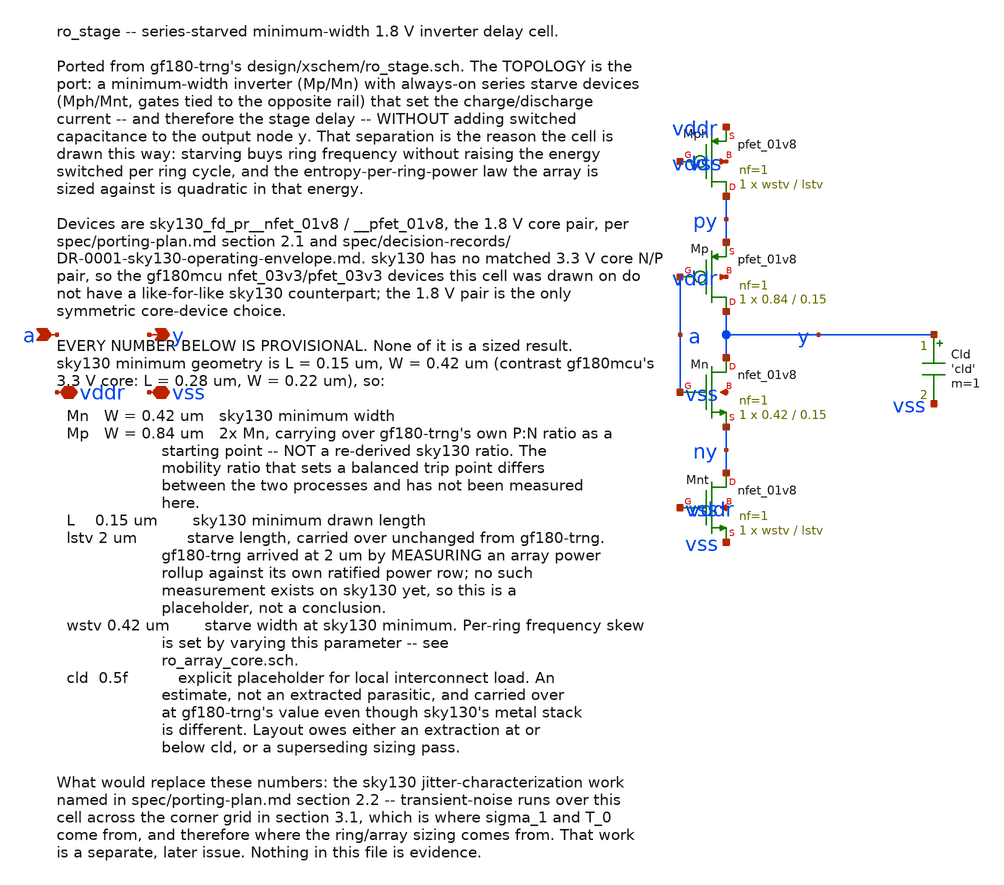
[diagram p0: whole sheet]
** sch_path: design/xschem/ro_stage.sch
**.subckt ro_stage a y vddr vss
*.ipin a
*.opin y
*.iopin vddr
*.iopin vss
XMph py vss vddr vddr sky130_fd_pr__pfet_01v8 L=lstv W=wstv nf=1 ad='int((nf+1)/2) * W/nf * 0.29' as='int((nf+2)/2) * W/nf * 0.29'
+ pd='2*int((nf+1)/2) * (W/nf + 0.29)' ps='2*int((nf+2)/2) * (W/nf + 0.29)' nrd='0.29 / W' nrs='0.29 / W'
+ sa=0 sb=0 sd=0 mult=1 m=1
XMp y a py vddr sky130_fd_pr__pfet_01v8 L=0.15 W=0.84 nf=1 ad='int((nf+1)/2) * W/nf * 0.29' as='int((nf+2)/2) * W/nf * 0.29'
+ pd='2*int((nf+1)/2) * (W/nf + 0.29)' ps='2*int((nf+2)/2) * (W/nf + 0.29)' nrd='0.29 / W' nrs='0.29 / W'
+ sa=0 sb=0 sd=0 mult=1 m=1
XMn y a ny vss sky130_fd_pr__nfet_01v8 L=0.15 W=0.42 nf=1 ad='int((1 + 1)/2) * 0.42 / 1 * 0.29' as='int((1 + 2)/2) * 0.42 / 1 * 0.29'
+ pd='2*int((1 + 1)/2) * (0.42 / 1 + 0.29)' ps='2*int((1 + 2)/2) * (0.42 / 1 + 0.29)' nrd='0.29 / 0.42 '
+ nrs='0.29 / 0.42 ' sa=0 sb=0 sd=0 mult=1 m=1
XMnt ny vddr vss vss sky130_fd_pr__nfet_01v8 L=lstv W=wstv nf=1 ad='int((1 + 1)/2) * wstv / 1 * 0.29'
+ as='int((1 + 2)/2) * wstv / 1 * 0.29' pd='2*int((1 + 1)/2) * (wstv / 1 + 0.29)' ps='2*int((1 + 2)/2) * (wstv / 1 + 0.29)'
+ nrd='0.29 / wstv ' nrs='0.29 / wstv ' sa=0 sb=0 sd=0 mult=1 m=1
Cld y vss 'cld' m=1
**.ends
.end
